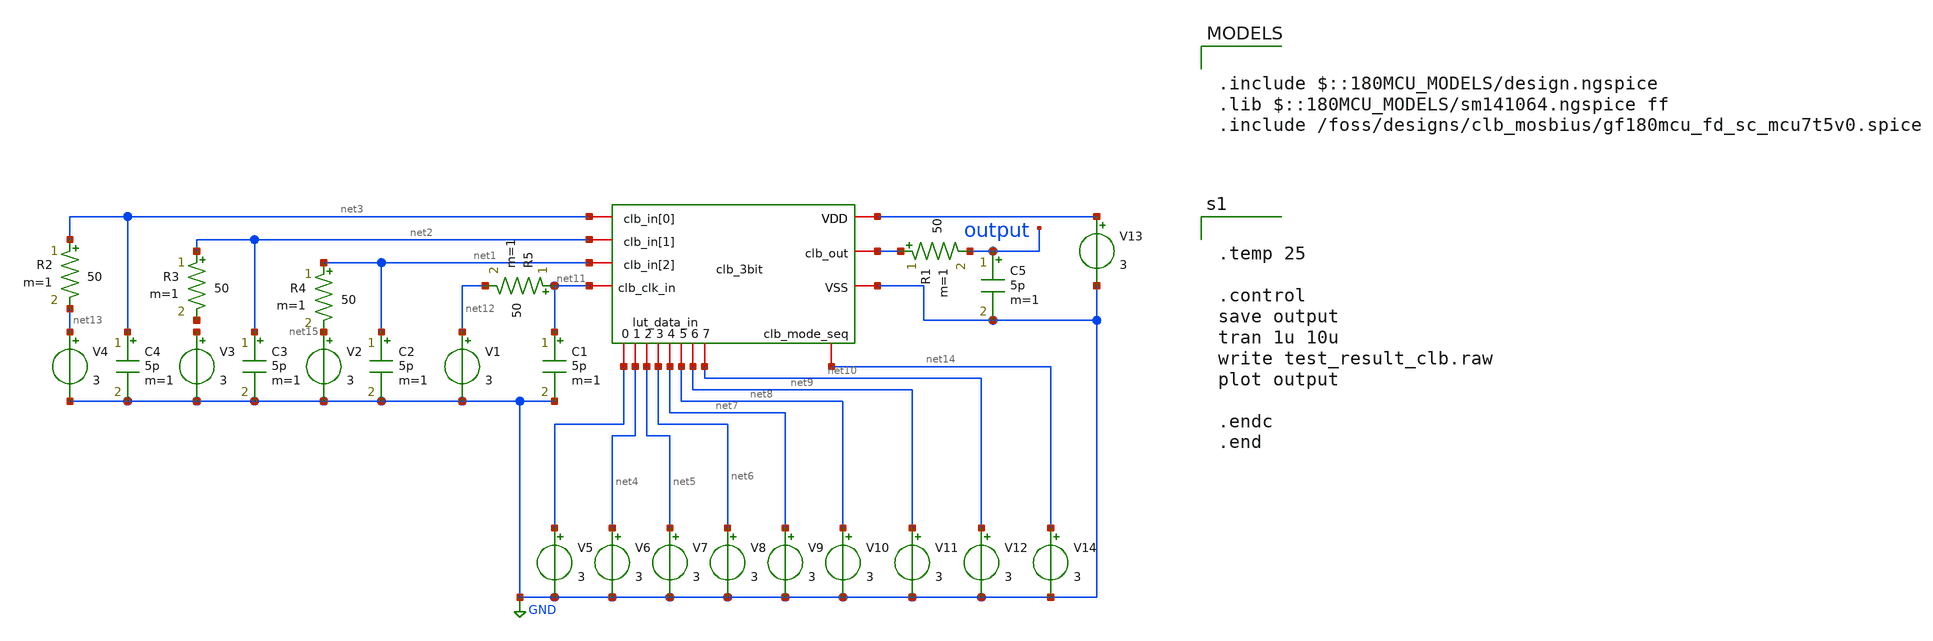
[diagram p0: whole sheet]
** sch_path: designs/digital/clb_mosbius/clb_3bit_tb.sch
**.subckt clb_3bit_tb
x1 GND net2 net2 net3 net3 net2 net2 net1 net11 net4 net5 net6 net7 net8 net9 net10 net14 clb_3bit
C1 net11 GND 5p m=1
C2 net1 GND 5p m=1
C3 net2 GND 5p m=1
C4 net3 GND 5p m=1
V1 net12 GND 3
V2 net15 GND 3
V3 net16 GND 3
V4 net13 GND 3
V5 net2 GND 3
V6 net4 GND 3
V7 net5 GND 3
V8 net6 GND 3
V9 net7 GND 3
V10 net8 GND 3
V11 net9 GND 3
V12 net10 GND 3
V13 net2 GND 3
C5 output GND 5p m=1
R1 net2 output 50 m=1
R2 net3 net13 50 m=1
R3 net2 net17 50 m=1
R4 net1 net15 50 m=1
R5 net11 net12 50 m=1
V14 net14 GND 3
**** begin user architecture code

.include $::180MCU_MODELS/design.ngspice
.lib $::180MCU_MODELS/sm141064.ngspice ff
.include /foss/designs/clb_mosbius/gf180mcu_fd_sc_mcu7t5v0.spice



.temp 25

.control
save output
tran 1u 10u
write test_result_clb.raw
plot output

.endc
.end


**** end user architecture code
**.ends

* expanding   symbol:  clb_mosbius/clb_3bit.sym # of pins=21
** sym_path: designs/digital/clb_mosbius/clb_3bit.sym
.include /foss/designs/clb_mosbius/clb_3bit.spice
.GLOBAL GND
.end
